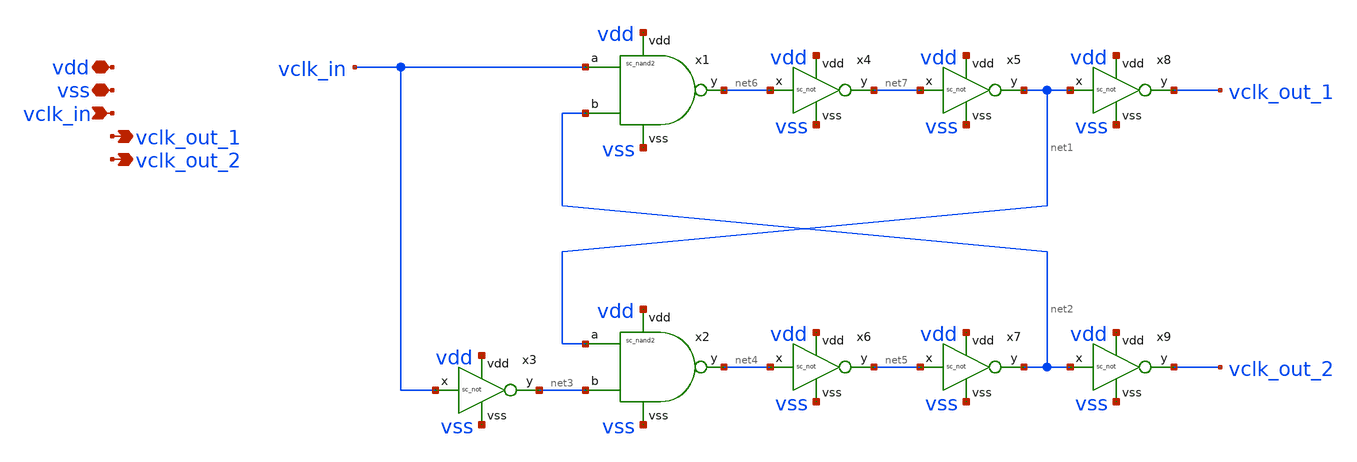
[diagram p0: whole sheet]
** sch_path: xschem/tl_nooverlap.sch
**.subckt tl_nooverlap vdd vss vclk_in vclk_out_1 vclk_out_2
*.iopin vdd
*.iopin vss
*.ipin vclk_in
*.opin vclk_out_1
*.opin vclk_out_2
x1 vclk_in net2 net6 vdd vss sc_nand2
x2 net1 net3 net4 vdd vss sc_nand2
x3 vdd vss vclk_in net3 sc_not
x4 vdd vss net6 net7 sc_not
x5 vdd vss net7 net1 sc_not
x6 vdd vss net4 net5 sc_not
x7 vdd vss net5 net2 sc_not
x8 vdd vss net1 vclk_out_1 sc_not
x9 vdd vss net2 vclk_out_2 sc_not
**.ends

* expanding   symbol:  sc_nand2.sym # of pins=5
** sym_path: xschem/sc_nand2.sym
** sch_path: xschem/sc_nand2.sch
.subckt sc_nand2 a b y vdd vss
*.iopin vdd
*.iopin vss
*.ipin a
*.opin y
*.ipin b
XM1 y a vdd vdd sky130_fd_pr__pfet_01v8 L=0.15 W=0.9 nf=1 ad='int((1 + 1)/2) * 0.9 / 1 * 0.29' as='int((1 + 2)/2) * 0.9 / 1 * 0.29'
+ pd='2*int((1 + 1)/2) * (0.9 / 1 + 0.29)' ps='2*int((1 + 2)/2) * (0.9 / 1 + 0.29)' nrd='0.29 / 0.9 ' nrs='0.29 / 0.9 '
+ sa=0 sb=0 sd=0 mult=1 m=1
XM2 y b vdd vdd sky130_fd_pr__pfet_01v8 L=0.15 W=0.9 nf=1 ad='int((1 + 1)/2) * 0.9 / 1 * 0.29' as='int((1 + 2)/2) * 0.9 / 1 * 0.29'
+ pd='2*int((1 + 1)/2) * (0.9 / 1 + 0.29)' ps='2*int((1 + 2)/2) * (0.9 / 1 + 0.29)' nrd='0.29 / 0.9 ' nrs='0.29 / 0.9 '
+ sa=0 sb=0 sd=0 mult=1 m=1
XM3 y a net1 vss sky130_fd_pr__nfet_01v8 L=0.15 W=0.45 nf=1 ad='int((nf+1)/2) * W/nf * 0.29' as='int((nf+2)/2) * W/nf * 0.29'
+ pd='2*int((nf+1)/2) * (W/nf + 0.29)' ps='2*int((nf+2)/2) * (W/nf + 0.29)' nrd='0.29 / W' nrs='0.29 / W'
+ sa=0 sb=0 sd=0 mult=1 m=1
XM4 net1 b vss vss sky130_fd_pr__nfet_01v8 L=0.15 W=0.45 nf=1 ad='int((nf+1)/2) * W/nf * 0.29' as='int((nf+2)/2) * W/nf * 0.29'
+ pd='2*int((nf+1)/2) * (W/nf + 0.29)' ps='2*int((nf+2)/2) * (W/nf + 0.29)' nrd='0.29 / W' nrs='0.29 / W'
+ sa=0 sb=0 sd=0 mult=1 m=1
.ends


* expanding   symbol:  sc_not.sym # of pins=4
** sym_path: xschem/sc_not.sym
** sch_path: xschem/sc_not.sch
.subckt sc_not vdd vss x y
*.iopin vdd
*.iopin vss
*.ipin x
*.opin y
XM1 y x vdd vdd sky130_fd_pr__pfet_01v8 L=0.15 W=0.9 nf=1 ad='int((1 + 1)/2) * 0.9 / 1 * 0.29' as='int((1 + 2)/2) * 0.9 / 1 * 0.29'
+ pd='2*int((1 + 1)/2) * (0.9 / 1 + 0.29)' ps='2*int((1 + 2)/2) * (0.9 / 1 + 0.29)' nrd='0.29 / 0.9 ' nrs='0.29 / 0.9 '
+ sa=0 sb=0 sd=0 mult=2 m=2
XM2 y x vss vss sky130_fd_pr__nfet_01v8 L=0.15 W=0.45 nf=1 ad='int((nf+1)/2) * W/nf * 0.29' as='int((nf+2)/2) * W/nf * 0.29'
+ pd='2*int((nf+1)/2) * (W/nf + 0.29)' ps='2*int((nf+2)/2) * (W/nf + 0.29)' nrd='0.29 / W' nrs='0.29 / W'
+ sa=0 sb=0 sd=0 mult=2 m=2
.ends

.end
